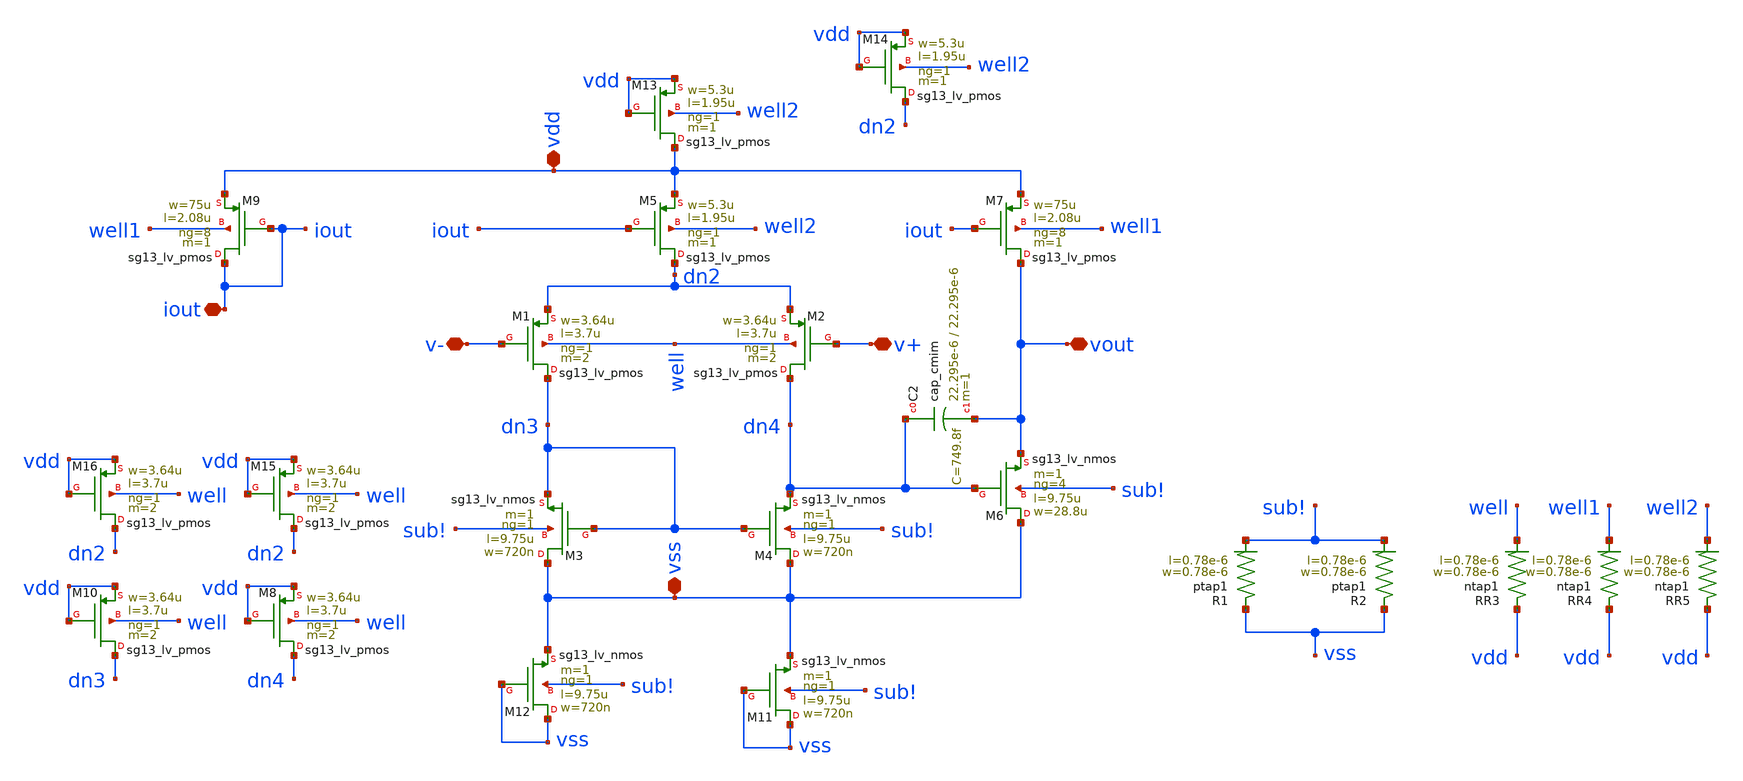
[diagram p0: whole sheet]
** sch_path: modules/module_1_bandgap_reference/part_3_layout/OTA_layout/full_OTA/schematic_mod/two_stage_OTA_layout.sch
**.subckt two_stage_OTA_layout v- v+ vss vdd iout vout
*.iopin v-
*.iopin v+
*.iopin vss
*.iopin vdd
*.iopin iout
*.iopin vout
XM4 vss dn3 dn4 sub! sg13_lv_nmos w=720n l=9.75u ng=1 m=1 mm_ok=1
XM3 vss dn3 dn3 sub! sg13_lv_nmos w=720n l=9.75u ng=1 m=1 mm_ok=1
XM1 dn3 v- dn2 well sg13_lv_pmos w=3.64u l=3.7u ng=1 m=2 mm_ok=1
XM2 dn4 v+ dn2 well sg13_lv_pmos w=3.64u l=3.7u ng=1 m=2 mm_ok=1
XM5 dn2 iout vdd well2 sg13_lv_pmos w=5.3u l=1.95u ng=1 m=1 mm_ok=1
XM7 vout iout vdd well1 sg13_lv_pmos w=75u l=2.08u ng=8 m=1 mm_ok=1
XM6 vss dn4 vout sub! sg13_lv_nmos w=28.8u l=9.75u ng=4 m=1 mm_ok=1
XM9 iout iout vdd well1 sg13_lv_pmos w=75u l=2.08u ng=8 m=1 mm_ok=1
XC2 dn4 vout cap_cmim w=22.295e-6 l=22.295e-6 m=1 mm_ok=1
XM8 dn4 vdd vdd well sg13_lv_pmos w=3.64u l=3.7u ng=1 m=2 mm_ok=1
XM10 dn3 vdd vdd well sg13_lv_pmos w=3.64u l=3.7u ng=1 m=2 mm_ok=1
XM11 vss vss vss sub! sg13_lv_nmos w=720n l=9.75u ng=1 m=1 mm_ok=1
XM12 vss vss vss sub! sg13_lv_nmos w=720n l=9.75u ng=1 m=1 mm_ok=1
XR1 vss sub! ptap1 R=262.8 w=0.78e-6 l=0.78e-6
XR2 vss sub! ptap1 R=262.8 w=0.78e-6 l=0.78e-6
XR3 vdd well ntap1 R=262.8 w=0.78e-6 l=0.78e-6
XR4 vdd well1 ntap1 R=262.8 w=0.78e-6 l=0.78e-6
XR5 vdd well2 ntap1 R=262.8 w=0.78e-6 l=0.78e-6
XM13 vdd vdd vdd well2 sg13_lv_pmos w=5.3u l=1.95u ng=1 m=1 mm_ok=1
XM14 dn2 vdd vdd well2 sg13_lv_pmos w=5.3u l=1.95u ng=1 m=1 mm_ok=1
XM15 dn2 vdd vdd well sg13_lv_pmos w=3.64u l=3.7u ng=1 m=2 mm_ok=1
XM16 dn2 vdd vdd well sg13_lv_pmos w=3.64u l=3.7u ng=1 m=2 mm_ok=1
**.ends
.end
